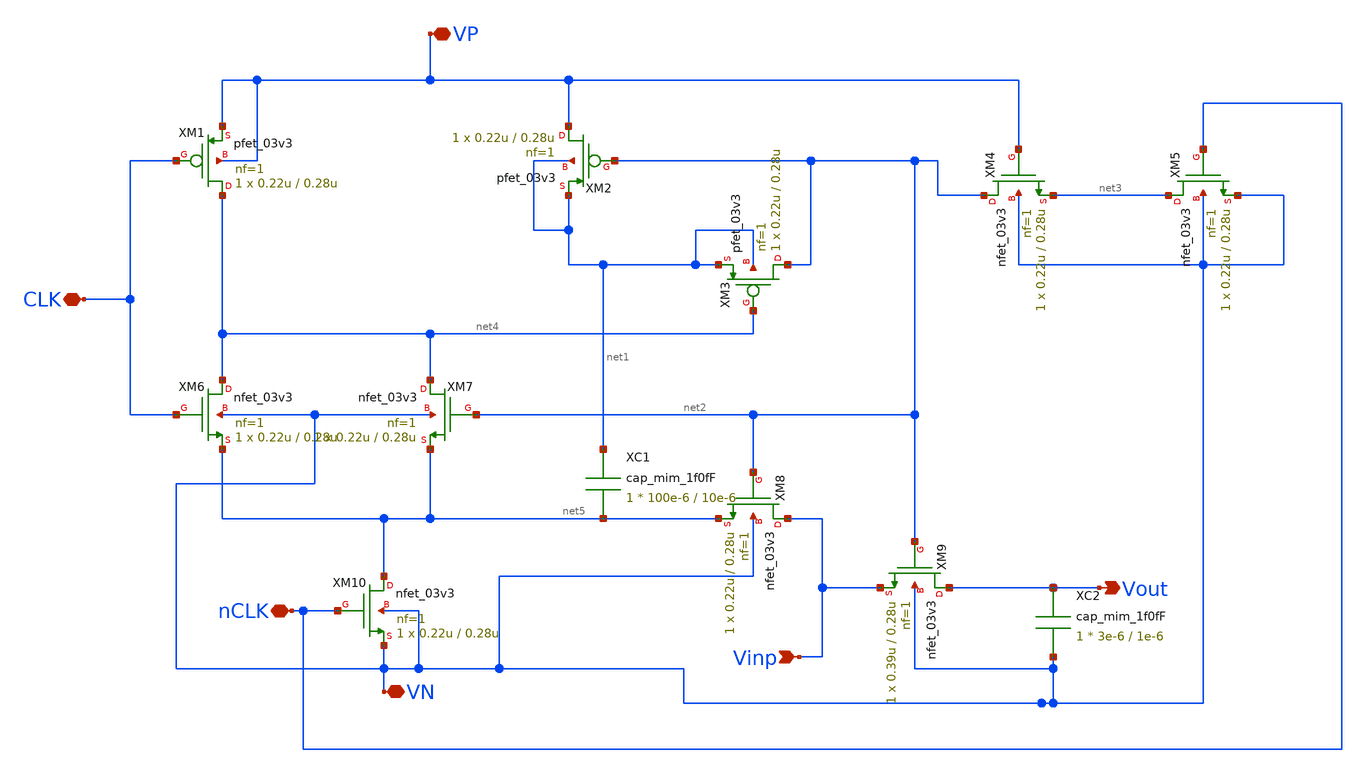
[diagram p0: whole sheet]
** sch_path: adc_sar_sample_and_hole.sch
**.subckt adc_sar_sample_and_hole Vinp Vout VP CLK nCLK VN
*.ipin Vinp
*.opin Vout
*.iopin VP
*.iopin CLK
*.iopin nCLK
*.iopin VN
XM1 net4 CLK VP VP pfet_03v3 L=0.28u W=0.22u nf=1 ad='int((nf+1)/2) * W/nf * 0.18u' as='int((nf+2)/2) * W/nf * 0.18u'
+ pd='2*int((nf+1)/2) * (W/nf + 0.18u)' ps='2*int((nf+2)/2) * (W/nf + 0.18u)' nrd='0.18u / W' nrs='0.18u / W'
+ sa=0 sb=0 sd=0 m=1
XM2 VP net2 net1 net1 pfet_03v3 L=0.28u W=0.22u nf=1 ad='int((nf+1)/2) * W/nf * 0.18u' as='int((nf+2)/2) * W/nf * 0.18u'
+ pd='2*int((nf+1)/2) * (W/nf + 0.18u)' ps='2*int((nf+2)/2) * (W/nf + 0.18u)' nrd='0.18u / W' nrs='0.18u / W'
+ sa=0 sb=0 sd=0 m=1
XM3 net2 net4 net1 net1 pfet_03v3 L=0.28u W=0.22u nf=1 ad='int((nf+1)/2) * W/nf * 0.18u' as='int((nf+2)/2) * W/nf * 0.18u'
+ pd='2*int((nf+1)/2) * (W/nf + 0.18u)' ps='2*int((nf+2)/2) * (W/nf + 0.18u)' nrd='0.18u / W' nrs='0.18u / W'
+ sa=0 sb=0 sd=0 m=1
XM4 net2 VP net3 VN nfet_03v3 L=0.28u W=0.22u nf=1 ad='int((nf+1)/2) * W/nf * 0.18u' as='int((nf+2)/2) * W/nf * 0.18u'
+ pd='2*int((nf+1)/2) * (W/nf + 0.18u)' ps='2*int((nf+2)/2) * (W/nf + 0.18u)' nrd='0.18u / W' nrs='0.18u / W'
+ sa=0 sb=0 sd=0 m=1
XM5 net3 nCLK VN VN nfet_03v3 L=0.28u W=0.22u nf=1 ad='int((nf+1)/2) * W/nf * 0.18u' as='int((nf+2)/2) * W/nf * 0.18u'
+ pd='2*int((nf+1)/2) * (W/nf + 0.18u)' ps='2*int((nf+2)/2) * (W/nf + 0.18u)' nrd='0.18u / W' nrs='0.18u / W'
+ sa=0 sb=0 sd=0 m=1
XM6 net4 CLK net5 VN nfet_03v3 L=0.28u W=0.22u nf=1 ad='int((nf+1)/2) * W/nf * 0.18u' as='int((nf+2)/2) * W/nf * 0.18u'
+ pd='2*int((nf+1)/2) * (W/nf + 0.18u)' ps='2*int((nf+2)/2) * (W/nf + 0.18u)' nrd='0.18u / W' nrs='0.18u / W'
+ sa=0 sb=0 sd=0 m=1
XM7 net4 net2 net5 VN nfet_03v3 L=0.28u W=0.22u nf=1 ad='int((nf+1)/2) * W/nf * 0.18u' as='int((nf+2)/2) * W/nf * 0.18u'
+ pd='2*int((nf+1)/2) * (W/nf + 0.18u)' ps='2*int((nf+2)/2) * (W/nf + 0.18u)' nrd='0.18u / W' nrs='0.18u / W'
+ sa=0 sb=0 sd=0 m=1
XM8 Vinp net2 net5 VN nfet_03v3 L=0.28u W=0.22u nf=1 ad='int((nf+1)/2) * W/nf * 0.18u' as='int((nf+2)/2) * W/nf * 0.18u'
+ pd='2*int((nf+1)/2) * (W/nf + 0.18u)' ps='2*int((nf+2)/2) * (W/nf + 0.18u)' nrd='0.18u / W' nrs='0.18u / W'
+ sa=0 sb=0 sd=0 m=1
XM9 Vout net2 Vinp VN nfet_03v3 L=0.28u W=0.39u nf=1 ad='int((nf+1)/2) * W/nf * 0.18u' as='int((nf+2)/2) * W/nf * 0.18u'
+ pd='2*int((nf+1)/2) * (W/nf + 0.18u)' ps='2*int((nf+2)/2) * (W/nf + 0.18u)' nrd='0.18u / W' nrs='0.18u / W'
+ sa=0 sb=0 sd=0 m=1
XC1 net1 net5 cap_mim_1f0fF c_width=100e-6 c_length=10e-6 m=1
XC2 Vout VN cap_mim_1f0fF c_width=3e-6 c_length=1e-6 m=1
XM10 net5 nCLK VN VN nfet_03v3 L=0.28u W=0.22u nf=1 ad='int((nf+1)/2) * W/nf * 0.18u' as='int((nf+2)/2) * W/nf * 0.18u'
+ pd='2*int((nf+1)/2) * (W/nf + 0.18u)' ps='2*int((nf+2)/2) * (W/nf + 0.18u)' nrd='0.18u / W' nrs='0.18u / W'
+ sa=0 sb=0 sd=0 m=1
**.ends
.end
